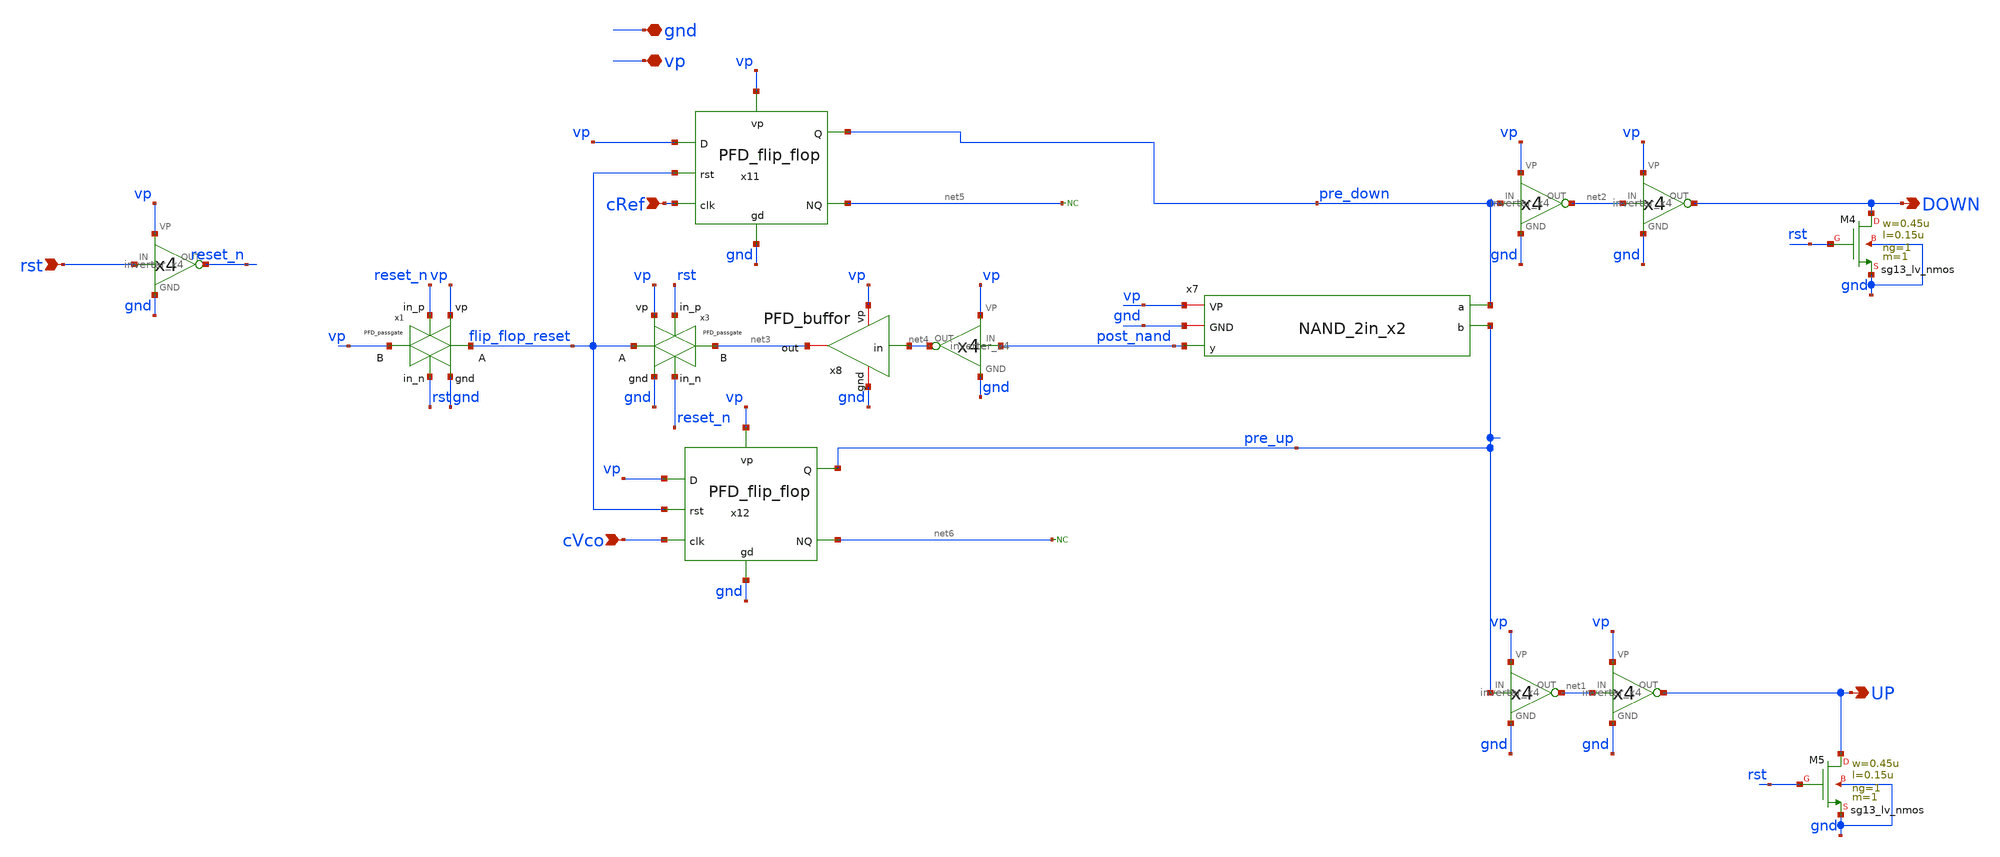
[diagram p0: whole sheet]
** sch_path: schematics/PFD/PFD_cell_2.sch
**.subckt PFD_cell_2 gnd vp cRef cVco rst UP DOWN
*.iopin gnd
*.iopin vp
*.ipin cRef
*.ipin cVco
*.ipin rst
*.opin UP
*.opin DOWN
x9 rst reset_n vp gnd inverter_x4
XM4 DOWN rst gnd gnd sg13_lv_nmos w=0.45u l=0.15u ng=1 m=1 mm_ok=1
XM5 UP rst gnd gnd sg13_lv_nmos w=0.45u l=0.15u ng=1 m=1 mm_ok=1
x4 net2 DOWN vp gnd inverter_x4
x6 net1 UP vp gnd inverter_x4
x2 pre_down net2 vp gnd inverter_x4
x5 pre_up net1 vp gnd inverter_x4
x1 rst vp flip_flop_reset vp gnd reset_n PFD_passgate
x3 reset_n vp flip_flop_reset net3 gnd rst PFD_passgate
x7 vp gnd pre_down post_nand pre_up NAND_2in_x2
* noconn #net5
x8 gnd vp net3 net4 PFD_buffor
x10 post_nand net4 vp gnd inverter_x4
x11 cRef flip_flop_reset vp pre_down net5 vp gnd PFD_flip_flop
x12 cVco flip_flop_reset vp pre_up net6 vp gnd PFD_flip_flop
* noconn #net6
**.ends
.end
